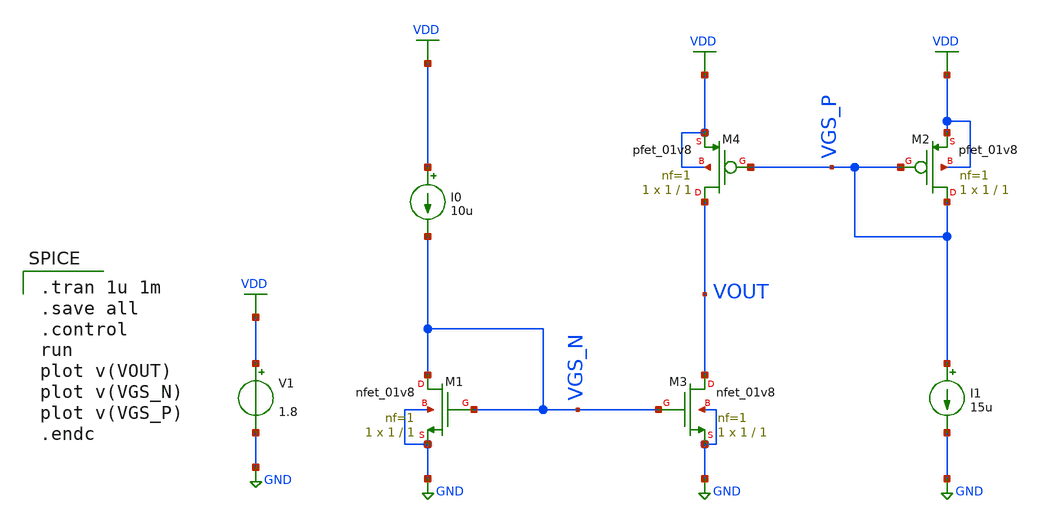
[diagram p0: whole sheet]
** sch_path: Circuits/Examples/Analog/Current_Comparison/Current_Comp.sch
**.subckt Current_Comp
V1 VDD GND 1.8
XM1 VGS_N VGS_N GND GND sky130_fd_pr__nfet_01v8 L=1 W=1 nf=1 ad='int((nf+1)/2) * W/nf * 0.29' as='int((nf+2)/2) * W/nf * 0.29'
+ pd='2*int((nf+1)/2) * (W/nf + 0.29)' ps='2*int((nf+2)/2) * (W/nf + 0.29)' nrd='0.29 / W' nrs='0.29 / W'
+ sa=0 sb=0 sd=0 mult=1 m=1
XM3 VOUT VGS_N GND GND sky130_fd_pr__nfet_01v8 L=1 W=1 nf=1 ad='int((nf+1)/2) * W/nf * 0.29' as='int((nf+2)/2) * W/nf * 0.29'
+ pd='2*int((nf+1)/2) * (W/nf + 0.29)' ps='2*int((nf+2)/2) * (W/nf + 0.29)' nrd='0.29 / W' nrs='0.29 / W'
+ sa=0 sb=0 sd=0 mult=1 m=1
XM4 VOUT VGS_P VDD VDD sky130_fd_pr__pfet_01v8 L=1 W=1 nf=1 ad='int((nf+1)/2) * W/nf * 0.29' as='int((nf+2)/2) * W/nf * 0.29'
+ pd='2*int((nf+1)/2) * (W/nf + 0.29)' ps='2*int((nf+2)/2) * (W/nf + 0.29)' nrd='0.29 / W' nrs='0.29 / W'
+ sa=0 sb=0 sd=0 mult=1 m=1
I0 VDD VGS_N 10u
I1 VGS_P GND 15u
XM2 VGS_P VGS_P VDD VDD sky130_fd_pr__pfet_01v8 L=1 W=1 nf=1 ad='int((nf+1)/2) * W/nf * 0.29' as='int((nf+2)/2) * W/nf * 0.29'
+ pd='2*int((nf+1)/2) * (W/nf + 0.29)' ps='2*int((nf+2)/2) * (W/nf + 0.29)' nrd='0.29 / W' nrs='0.29 / W'
+ sa=0 sb=0 sd=0 mult=1 m=1
**** begin user architecture code
 ** manual skywater pdks install (with patches applied)
* .lib $::SKYWATER_MODELS/models/sky130.lib.spice tt

** opencircuitdesign pdks install
.lib $::SKYWATER_MODELS/sky130.lib.spice tt

.param mc_mm_switch=0
.param mc_pr_switch=0


.tran 1u 1m
.save all
.control
run
plot v(VOUT)
plot v(VGS_N)
plot v(VGS_P)
.endc


**** end user architecture code
**.ends
.GLOBAL GND
.GLOBAL VDD
.end
